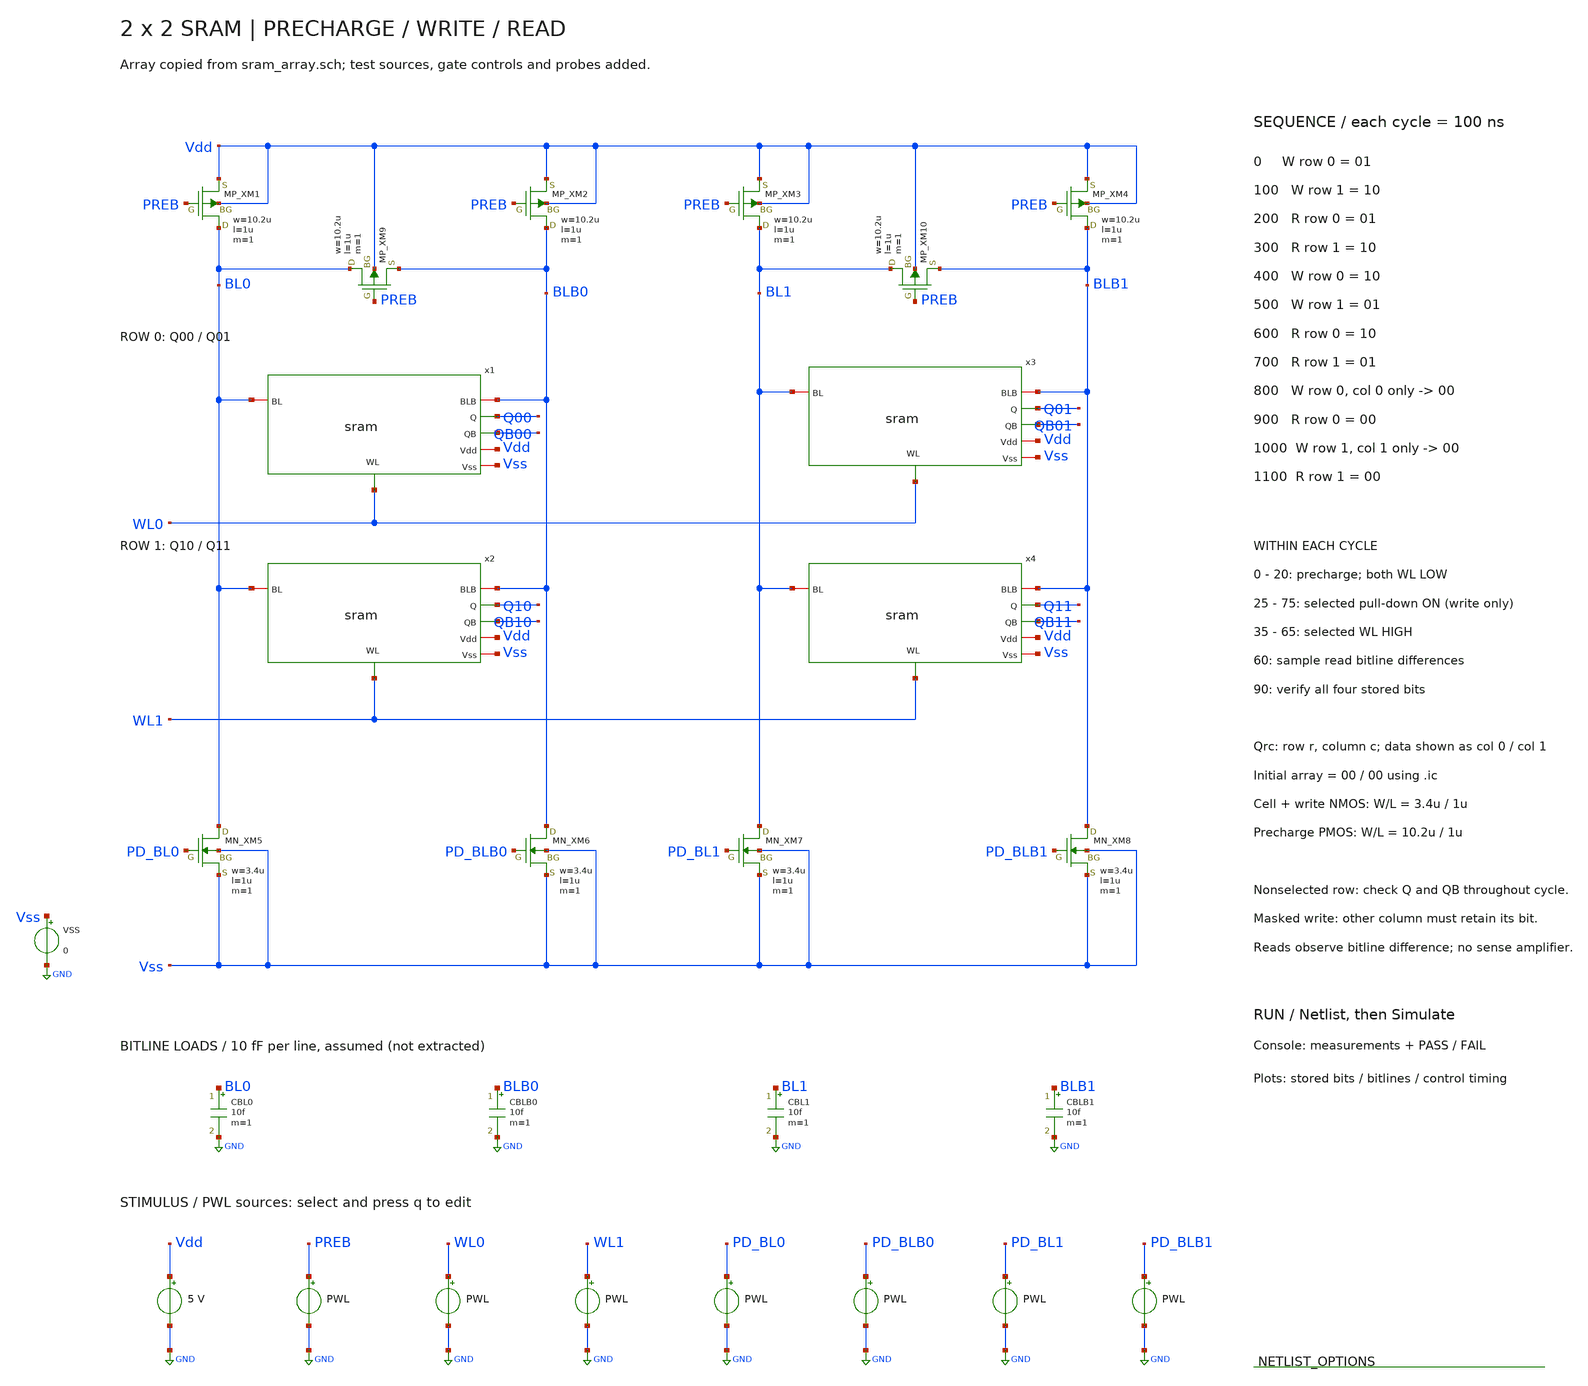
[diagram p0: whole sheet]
** sch_path: member_project/SRAM/PenguinEino/learning/schematics/sram_tb_array.sch
**.subckt sram_tb_array
x1 WL0 Vdd BLB0 Q00 QB00 BL0 Vss sram
x2 WL1 Vdd BLB0 Q10 QB10 BL0 Vss sram
x3 WL0 Vdd BLB1 Q01 QB01 BL1 Vss sram
x4 WL1 Vdd BLB1 Q11 QB11 BL1 Vss sram
XXM1 BL0 PREB Vdd Vdd PMOS w=10.2u l=1u nrd=0 nrs=0 m=1
XXM2 BLB0 PREB Vdd Vdd PMOS w=10.2u l=1u nrd=0 nrs=0 m=1
XXM3 BL1 PREB Vdd Vdd PMOS w=10.2u l=1u nrd=0 nrs=0 m=1
XXM4 BLB1 PREB Vdd Vdd PMOS w=10.2u l=1u nrd=0 nrs=0 m=1
XXM5 BL0 PD_BL0 Vss Vss NMOS w=3.4u l=1u nrd=0 nrs=0 m=1
XXM6 BLB0 PD_BLB0 Vss Vss NMOS w=3.4u l=1u nrd=0 nrs=0 m=1
XXM7 BL1 PD_BL1 Vss Vss NMOS w=3.4u l=1u nrd=0 nrs=0 m=1
XXM8 BLB1 PD_BLB1 Vss Vss NMOS w=3.4u l=1u nrd=0 nrs=0 m=1
XXM9 BL0 PREB BLB0 Vdd PMOS w=10.2u l=1u nrd=0 nrs=0 m=1
XXM10 BL1 PREB BLB1 Vdd PMOS w=10.2u l=1u nrd=0 nrs=0 m=1
VSS Vss GND 0
CBL0 BL0 GND 10f m=1
CBLB0 BLB0 GND 10f m=1
CBL1 BL1 GND 10f m=1
CBLB1 BLB1 GND 10f m=1
VVdd Vdd GND 5
VPREB PREB GND PWL(0n 0 20n 0 21n 5 100n 5 101n 0 120n 0 121n 5 200n 5 201n 0 220n 0 221n 5 300n 5
+ 301n 0 320n 0 321n 5 400n 5 401n 0 420n 0 421n 5 500n 5 501n 0 520n 0 521n 5 600n 5 601n 0 620n 0 621n 5
+ 700n 5 701n 0 720n 0 721n 5 800n 5 801n 0 820n 0 821n 5 900n 5 901n 0 920n 0 921n 5 1000n 5 1001n 0
+ 1020n 0 1021n 5 1100n 5 1101n 0 1120n 0 1121n 5 1200n 5)
VWL0 WL0 GND PWL(0n 0 35n 0 36n 5 65n 5 66n 0 235n 0 236n 5 265n 5 266n 0 435n 0 436n 5 465n 5 466n
+ 0 635n 0 636n 5 665n 5 666n 0 835n 0 836n 5 865n 5 866n 0 935n 0 936n 5 965n 5 966n 0 1200n 0)
VWL1 WL1 GND PWL(0n 0 135n 0 136n 5 165n 5 166n 0 335n 0 336n 5 365n 5 366n 0 535n 0 536n 5 565n 5
+ 566n 0 735n 0 736n 5 765n 5 766n 0 1035n 0 1036n 5 1065n 5 1066n 0 1135n 0 1136n 5 1165n 5 1166n 0 1200n
+ 0)
VPD_BL0 PD_BL0 GND PWL(0n 0 25n 0 26n 5 75n 5 76n 0 525n 0 526n 5 575n 5 576n 0 825n 0 826n 5 875n 5
+ 876n 0 1200n 0)
VPD_BLB0 PD_BLB0 GND PWL(0n 0 125n 0 126n 5 175n 5 176n 0 425n 0 426n 5 475n 5 476n 0 1200n 0)
VPD_BL1 PD_BL1 GND PWL(0n 0 125n 0 126n 5 175n 5 176n 0 425n 0 426n 5 475n 5 476n 0 1025n 0 1026n 5
+ 1075n 5 1076n 0 1200n 0)
VPD_BLB1 PD_BLB1 GND PWL(0n 0 25n 0 26n 5 75n 5 76n 0 525n 0 526n 5 575n 5 576n 0 1200n 0)
**** begin user architecture code
 .include $::LIB/ip62_models

* Nominal functional test. Qrc = row r, column c.
.ic v(Q00)=0 v(QB00)=5 v(Q01)=0 v(QB01)=5 v(Q10)=0 v(QB10)=5 v(Q11)=0 v(QB11)=5
.control
save all
tran 0.05n 1200n
let failures = 0
let diff0 = v(BL0)-v(BLB0)
let diff1 = v(BL1)-v(BLB1)
echo CYCLE_0: W row_0
meas tran nslo_0_0 max v(Q10) from=0n to=99n
meas tran nshi_0_0 min v(QB10) from=0n to=99n
if nslo_0_0 > 0.5 or nshi_0_0 < 4.5
 let failures = failures + 1
end
meas tran nslo_0_1 max v(Q11) from=0n to=99n
meas tran nshi_0_1 min v(QB11) from=0n to=99n
if nslo_0_1 > 0.5 or nshi_0_1 < 4.5
 let failures = failures + 1
end
meas tran q_0_00 find v(Q00) at=90n
meas tran qb_0_00 find v(QB00) at=90n
if q_0_00 > 0.5 or qb_0_00 < 4.5
 let failures = failures + 1
end
meas tran q_0_01 find v(Q01) at=90n
meas tran qb_0_01 find v(QB01) at=90n
if q_0_01 < 4.5 or qb_0_01 > 0.5
 let failures = failures + 1
end
meas tran q_0_10 find v(Q10) at=90n
meas tran qb_0_10 find v(QB10) at=90n
if q_0_10 > 0.5 or qb_0_10 < 4.5
 let failures = failures + 1
end
meas tran q_0_11 find v(Q11) at=90n
meas tran qb_0_11 find v(QB11) at=90n
if q_0_11 > 0.5 or qb_0_11 < 4.5
 let failures = failures + 1
end
echo CYCLE_1: W row_1
meas tran nslo_1_0 max v(Q00) from=100n to=199n
meas tran nshi_1_0 min v(QB00) from=100n to=199n
if nslo_1_0 > 0.5 or nshi_1_0 < 4.5
 let failures = failures + 1
end
meas tran nslo_1_1 max v(QB01) from=100n to=199n
meas tran nshi_1_1 min v(Q01) from=100n to=199n
if nslo_1_1 > 0.5 or nshi_1_1 < 4.5
 let failures = failures + 1
end
meas tran q_1_00 find v(Q00) at=190n
meas tran qb_1_00 find v(QB00) at=190n
if q_1_00 > 0.5 or qb_1_00 < 4.5
 let failures = failures + 1
end
meas tran q_1_01 find v(Q01) at=190n
meas tran qb_1_01 find v(QB01) at=190n
if q_1_01 < 4.5 or qb_1_01 > 0.5
 let failures = failures + 1
end
meas tran q_1_10 find v(Q10) at=190n
meas tran qb_1_10 find v(QB10) at=190n
if q_1_10 < 4.5 or qb_1_10 > 0.5
 let failures = failures + 1
end
meas tran q_1_11 find v(Q11) at=190n
meas tran qb_1_11 find v(QB11) at=190n
if q_1_11 > 0.5 or qb_1_11 < 4.5
 let failures = failures + 1
end
echo CYCLE_2: R row_0
meas tran nslo_2_0 max v(QB10) from=200n to=299n
meas tran nshi_2_0 min v(Q10) from=200n to=299n
if nslo_2_0 > 0.5 or nshi_2_0 < 4.5
 let failures = failures + 1
end
meas tran nslo_2_1 max v(Q11) from=200n to=299n
meas tran nshi_2_1 min v(QB11) from=200n to=299n
if nslo_2_1 > 0.5 or nshi_2_1 < 4.5
 let failures = failures + 1
end
meas tran rd_2_0 find diff0 at=260n
if rd_2_0 > -0.5
 let failures = failures + 1
end
meas tran rd_2_1 find diff1 at=260n
if rd_2_1 < 0.5
 let failures = failures + 1
end
meas tran q_2_00 find v(Q00) at=290n
meas tran qb_2_00 find v(QB00) at=290n
if q_2_00 > 0.5 or qb_2_00 < 4.5
 let failures = failures + 1
end
meas tran q_2_01 find v(Q01) at=290n
meas tran qb_2_01 find v(QB01) at=290n
if q_2_01 < 4.5 or qb_2_01 > 0.5
 let failures = failures + 1
end
meas tran q_2_10 find v(Q10) at=290n
meas tran qb_2_10 find v(QB10) at=290n
if q_2_10 < 4.5 or qb_2_10 > 0.5
 let failures = failures + 1
end
meas tran q_2_11 find v(Q11) at=290n
meas tran qb_2_11 find v(QB11) at=290n
if q_2_11 > 0.5 or qb_2_11 < 4.5
 let failures = failures + 1
end
echo CYCLE_3: R row_1
meas tran nslo_3_0 max v(Q00) from=300n to=399n
meas tran nshi_3_0 min v(QB00) from=300n to=399n
if nslo_3_0 > 0.5 or nshi_3_0 < 4.5
 let failures = failures + 1
end
meas tran nslo_3_1 max v(QB01) from=300n to=399n
meas tran nshi_3_1 min v(Q01) from=300n to=399n
if nslo_3_1 > 0.5 or nshi_3_1 < 4.5
 let failures = failures + 1
end
meas tran rd_3_0 find diff0 at=360n
if rd_3_0 < 0.5
 let failures = failures + 1
end
meas tran rd_3_1 find diff1 at=360n
if rd_3_1 > -0.5
 let failures = failures + 1
end
meas tran q_3_00 find v(Q00) at=390n
meas tran qb_3_00 find v(QB00) at=390n
if q_3_00 > 0.5 or qb_3_00 < 4.5
 let failures = failures + 1
end
meas tran q_3_01 find v(Q01) at=390n
meas tran qb_3_01 find v(QB01) at=390n
if q_3_01 < 4.5 or qb_3_01 > 0.5
 let failures = failures + 1
end
meas tran q_3_10 find v(Q10) at=390n
meas tran qb_3_10 find v(QB10) at=390n
if q_3_10 < 4.5 or qb_3_10 > 0.5
 let failures = failures + 1
end
meas tran q_3_11 find v(Q11) at=390n
meas tran qb_3_11 find v(QB11) at=390n
if q_3_11 > 0.5 or qb_3_11 < 4.5
 let failures = failures + 1
end
echo CYCLE_4: W row_0
meas tran nslo_4_0 max v(QB10) from=400n to=499n
meas tran nshi_4_0 min v(Q10) from=400n to=499n
if nslo_4_0 > 0.5 or nshi_4_0 < 4.5
 let failures = failures + 1
end
meas tran nslo_4_1 max v(Q11) from=400n to=499n
meas tran nshi_4_1 min v(QB11) from=400n to=499n
if nslo_4_1 > 0.5 or nshi_4_1 < 4.5
 let failures = failures + 1
end
meas tran q_4_00 find v(Q00) at=490n
meas tran qb_4_00 find v(QB00) at=490n
if q_4_00 < 4.5 or qb_4_00 > 0.5
 let failures = failures + 1
end
meas tran q_4_01 find v(Q01) at=490n
meas tran qb_4_01 find v(QB01) at=490n
if q_4_01 > 0.5 or qb_4_01 < 4.5
 let failures = failures + 1
end
meas tran q_4_10 find v(Q10) at=490n
meas tran qb_4_10 find v(QB10) at=490n
if q_4_10 < 4.5 or qb_4_10 > 0.5
 let failures = failures + 1
end
meas tran q_4_11 find v(Q11) at=490n
meas tran qb_4_11 find v(QB11) at=490n
if q_4_11 > 0.5 or qb_4_11 < 4.5
 let failures = failures + 1
end
echo CYCLE_5: W row_1
meas tran nslo_5_0 max v(QB00) from=500n to=599n
meas tran nshi_5_0 min v(Q00) from=500n to=599n
if nslo_5_0 > 0.5 or nshi_5_0 < 4.5
 let failures = failures + 1
end
meas tran nslo_5_1 max v(Q01) from=500n to=599n
meas tran nshi_5_1 min v(QB01) from=500n to=599n
if nslo_5_1 > 0.5 or nshi_5_1 < 4.5
 let failures = failures + 1
end
meas tran q_5_00 find v(Q00) at=590n
meas tran qb_5_00 find v(QB00) at=590n
if q_5_00 < 4.5 or qb_5_00 > 0.5
 let failures = failures + 1
end
meas tran q_5_01 find v(Q01) at=590n
meas tran qb_5_01 find v(QB01) at=590n
if q_5_01 > 0.5 or qb_5_01 < 4.5
 let failures = failures + 1
end
meas tran q_5_10 find v(Q10) at=590n
meas tran qb_5_10 find v(QB10) at=590n
if q_5_10 > 0.5 or qb_5_10 < 4.5
 let failures = failures + 1
end
meas tran q_5_11 find v(Q11) at=590n
meas tran qb_5_11 find v(QB11) at=590n
if q_5_11 < 4.5 or qb_5_11 > 0.5
 let failures = failures + 1
end
echo CYCLE_6: R row_0
meas tran nslo_6_0 max v(Q10) from=600n to=699n
meas tran nshi_6_0 min v(QB10) from=600n to=699n
if nslo_6_0 > 0.5 or nshi_6_0 < 4.5
 let failures = failures + 1
end
meas tran nslo_6_1 max v(QB11) from=600n to=699n
meas tran nshi_6_1 min v(Q11) from=600n to=699n
if nslo_6_1 > 0.5 or nshi_6_1 < 4.5
 let failures = failures + 1
end
meas tran rd_6_0 find diff0 at=660n
if rd_6_0 < 0.5
 let failures = failures + 1
end
meas tran rd_6_1 find diff1 at=660n
if rd_6_1 > -0.5
 let failures = failures + 1
end
meas tran q_6_00 find v(Q00) at=690n
meas tran qb_6_00 find v(QB00) at=690n
if q_6_00 < 4.5 or qb_6_00 > 0.5
 let failures = failures + 1
end
meas tran q_6_01 find v(Q01) at=690n
meas tran qb_6_01 find v(QB01) at=690n
if q_6_01 > 0.5 or qb_6_01 < 4.5
 let failures = failures + 1
end
meas tran q_6_10 find v(Q10) at=690n
meas tran qb_6_10 find v(QB10) at=690n
if q_6_10 > 0.5 or qb_6_10 < 4.5
 let failures = failures + 1
end
meas tran q_6_11 find v(Q11) at=690n
meas tran qb_6_11 find v(QB11) at=690n
if q_6_11 < 4.5 or qb_6_11 > 0.5
 let failures = failures + 1
end
echo CYCLE_7: R row_1
meas tran nslo_7_0 max v(QB00) from=700n to=799n
meas tran nshi_7_0 min v(Q00) from=700n to=799n
if nslo_7_0 > 0.5 or nshi_7_0 < 4.5
 let failures = failures + 1
end
meas tran nslo_7_1 max v(Q01) from=700n to=799n
meas tran nshi_7_1 min v(QB01) from=700n to=799n
if nslo_7_1 > 0.5 or nshi_7_1 < 4.5
 let failures = failures + 1
end
meas tran rd_7_0 find diff0 at=760n
if rd_7_0 > -0.5
 let failures = failures + 1
end
meas tran rd_7_1 find diff1 at=760n
if rd_7_1 < 0.5
 let failures = failures + 1
end
meas tran q_7_00 find v(Q00) at=790n
meas tran qb_7_00 find v(QB00) at=790n
if q_7_00 < 4.5 or qb_7_00 > 0.5
 let failures = failures + 1
end
meas tran q_7_01 find v(Q01) at=790n
meas tran qb_7_01 find v(QB01) at=790n
if q_7_01 > 0.5 or qb_7_01 < 4.5
 let failures = failures + 1
end
meas tran q_7_10 find v(Q10) at=790n
meas tran qb_7_10 find v(QB10) at=790n
if q_7_10 > 0.5 or qb_7_10 < 4.5
 let failures = failures + 1
end
meas tran q_7_11 find v(Q11) at=790n
meas tran qb_7_11 find v(QB11) at=790n
if q_7_11 < 4.5 or qb_7_11 > 0.5
 let failures = failures + 1
end
echo CYCLE_8: W row_0
meas tran nslo_8_0 max v(Q10) from=800n to=899n
meas tran nshi_8_0 min v(QB10) from=800n to=899n
if nslo_8_0 > 0.5 or nshi_8_0 < 4.5
 let failures = failures + 1
end
meas tran nslo_8_1 max v(QB11) from=800n to=899n
meas tran nshi_8_1 min v(Q11) from=800n to=899n
if nslo_8_1 > 0.5 or nshi_8_1 < 4.5
 let failures = failures + 1
end
meas tran q_8_00 find v(Q00) at=890n
meas tran qb_8_00 find v(QB00) at=890n
if q_8_00 > 0.5 or qb_8_00 < 4.5
 let failures = failures + 1
end
meas tran q_8_01 find v(Q01) at=890n
meas tran qb_8_01 find v(QB01) at=890n
if q_8_01 > 0.5 or qb_8_01 < 4.5
 let failures = failures + 1
end
meas tran q_8_10 find v(Q10) at=890n
meas tran qb_8_10 find v(QB10) at=890n
if q_8_10 > 0.5 or qb_8_10 < 4.5
 let failures = failures + 1
end
meas tran q_8_11 find v(Q11) at=890n
meas tran qb_8_11 find v(QB11) at=890n
if q_8_11 < 4.5 or qb_8_11 > 0.5
 let failures = failures + 1
end
echo CYCLE_9: R row_0
meas tran nslo_9_0 max v(Q10) from=900n to=999n
meas tran nshi_9_0 min v(QB10) from=900n to=999n
if nslo_9_0 > 0.5 or nshi_9_0 < 4.5
 let failures = failures + 1
end
meas tran nslo_9_1 max v(QB11) from=900n to=999n
meas tran nshi_9_1 min v(Q11) from=900n to=999n
if nslo_9_1 > 0.5 or nshi_9_1 < 4.5
 let failures = failures + 1
end
meas tran rd_9_0 find diff0 at=960n
if rd_9_0 > -0.5
 let failures = failures + 1
end
meas tran rd_9_1 find diff1 at=960n
if rd_9_1 > -0.5
 let failures = failures + 1
end
meas tran q_9_00 find v(Q00) at=990n
meas tran qb_9_00 find v(QB00) at=990n
if q_9_00 > 0.5 or qb_9_00 < 4.5
 let failures = failures + 1
end
meas tran q_9_01 find v(Q01) at=990n
meas tran qb_9_01 find v(QB01) at=990n
if q_9_01 > 0.5 or qb_9_01 < 4.5
 let failures = failures + 1
end
meas tran q_9_10 find v(Q10) at=990n
meas tran qb_9_10 find v(QB10) at=990n
if q_9_10 > 0.5 or qb_9_10 < 4.5
 let failures = failures + 1
end
meas tran q_9_11 find v(Q11) at=990n
meas tran qb_9_11 find v(QB11) at=990n
if q_9_11 < 4.5 or qb_9_11 > 0.5
 let failures = failures + 1
end
echo CYCLE_10: W row_1
meas tran nslo_10_0 max v(Q00) from=1000n to=1099n
meas tran nshi_10_0 min v(QB00) from=1000n to=1099n
if nslo_10_0 > 0.5 or nshi_10_0 < 4.5
 let failures = failures + 1
end
meas tran nslo_10_1 max v(Q01) from=1000n to=1099n
meas tran nshi_10_1 min v(QB01) from=1000n to=1099n
if nslo_10_1 > 0.5 or nshi_10_1 < 4.5
 let failures = failures + 1
end
meas tran q_10_00 find v(Q00) at=1090n
meas tran qb_10_00 find v(QB00) at=1090n
if q_10_00 > 0.5 or qb_10_00 < 4.5
 let failures = failures + 1
end
meas tran q_10_01 find v(Q01) at=1090n
meas tran qb_10_01 find v(QB01) at=1090n
if q_10_01 > 0.5 or qb_10_01 < 4.5
 let failures = failures + 1
end
meas tran q_10_10 find v(Q10) at=1090n
meas tran qb_10_10 find v(QB10) at=1090n
if q_10_10 > 0.5 or qb_10_10 < 4.5
 let failures = failures + 1
end
meas tran q_10_11 find v(Q11) at=1090n
meas tran qb_10_11 find v(QB11) at=1090n
if q_10_11 > 0.5 or qb_10_11 < 4.5
 let failures = failures + 1
end
echo CYCLE_11: R row_1
meas tran nslo_11_0 max v(Q00) from=1100n to=1199n
meas tran nshi_11_0 min v(QB00) from=1100n to=1199n
if nslo_11_0 > 0.5 or nshi_11_0 < 4.5
 let failures = failures + 1
end
meas tran nslo_11_1 max v(Q01) from=1100n to=1199n
meas tran nshi_11_1 min v(QB01) from=1100n to=1199n
if nslo_11_1 > 0.5 or nshi_11_1 < 4.5
 let failures = failures + 1
end
meas tran rd_11_0 find diff0 at=1160n
if rd_11_0 > -0.5
 let failures = failures + 1
end
meas tran rd_11_1 find diff1 at=1160n
if rd_11_1 > -0.5
 let failures = failures + 1
end
meas tran q_11_00 find v(Q00) at=1190n
meas tran qb_11_00 find v(QB00) at=1190n
if q_11_00 > 0.5 or qb_11_00 < 4.5
 let failures = failures + 1
end
meas tran q_11_01 find v(Q01) at=1190n
meas tran qb_11_01 find v(QB01) at=1190n
if q_11_01 > 0.5 or qb_11_01 < 4.5
 let failures = failures + 1
end
meas tran q_11_10 find v(Q10) at=1190n
meas tran qb_11_10 find v(QB10) at=1190n
if q_11_10 > 0.5 or qb_11_10 < 4.5
 let failures = failures + 1
end
meas tran q_11_11 find v(Q11) at=1190n
meas tran qb_11_11 find v(QB11) at=1190n
if q_11_11 > 0.5 or qb_11_11 < 4.5
 let failures = failures + 1
end
if failures = 0
 echo PASS: writes, reads, masked writes and nonselected-row retention
else
 echo FAIL: array checks failed
 print failures
end
write sram_tb_array.raw
plot v(Q00) v(Q01) ylimit -0.5 5.5 title 'ROW 0: Q00 / Q01'
plot v(Q10) v(Q11) ylimit -0.5 5.5 title 'ROW 1: Q10 / Q11'
plot v(BL0) v(BLB0) ylimit -0.5 5.5 title 'COLUMN 0: BL / BLB'
plot v(BL1) v(BLB1) ylimit -0.5 5.5 title 'COLUMN 1: BL / BLB'
let PREB_T = v(PREB)/5+12
let WL0_T = v(WL0)/5+10
let WL1_T = v(WL1)/5+8
let PD_BL0_T = v(PD_BL0)/5+6
let PD_BLB0_T = v(PD_BLB0)/5+4
let PD_BL1_T = v(PD_BL1)/5+2
let PD_BLB1_T = v(PD_BLB1)/5+0
plot PREB_T WL0_T WL1_T PD_BL0_T PD_BLB0_T PD_BL1_T PD_BLB1_T ylimit -0.3 13.3 title 'CONTROLS: PREB +12 / WL0 +10 / WL1 +8 / PD_BL0 +6 / PD_BLB0 +4 / PD_BL1 +2 / PD_BLB1 +0'
.endc

**** end user architecture code
**.ends
.GLOBAL GND
.end
